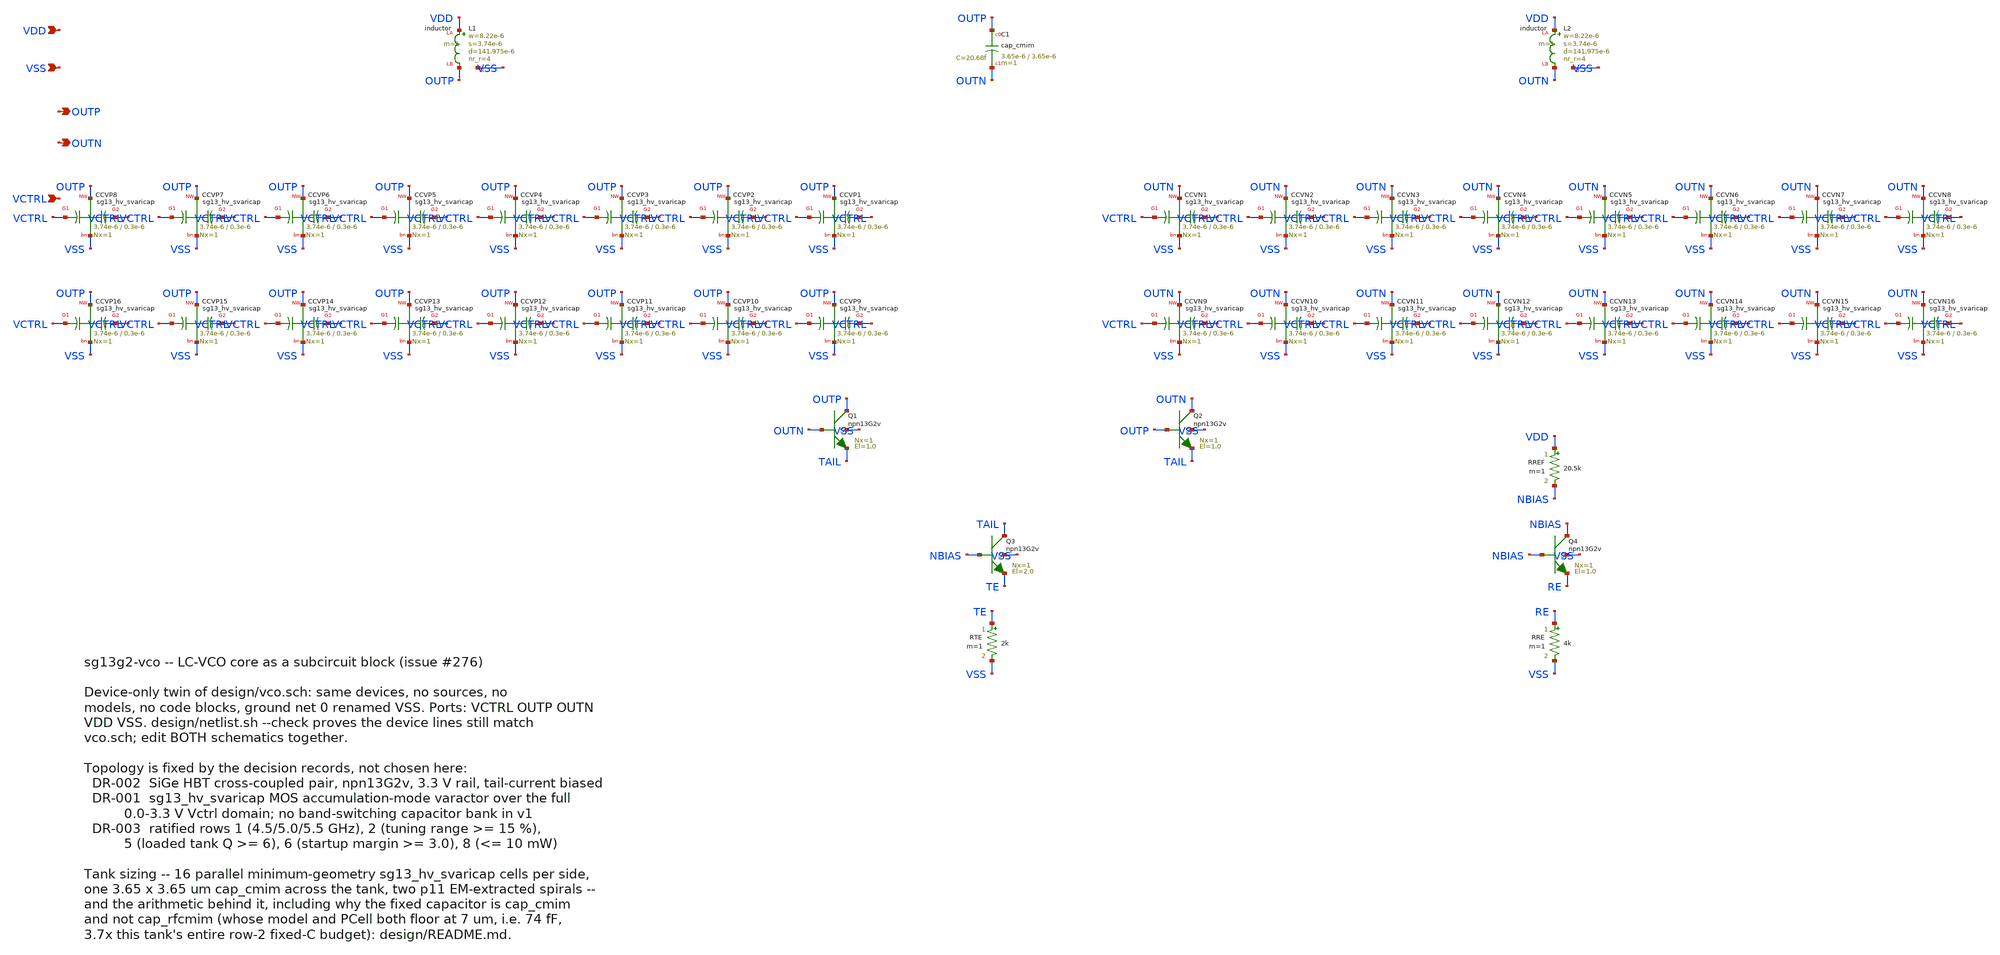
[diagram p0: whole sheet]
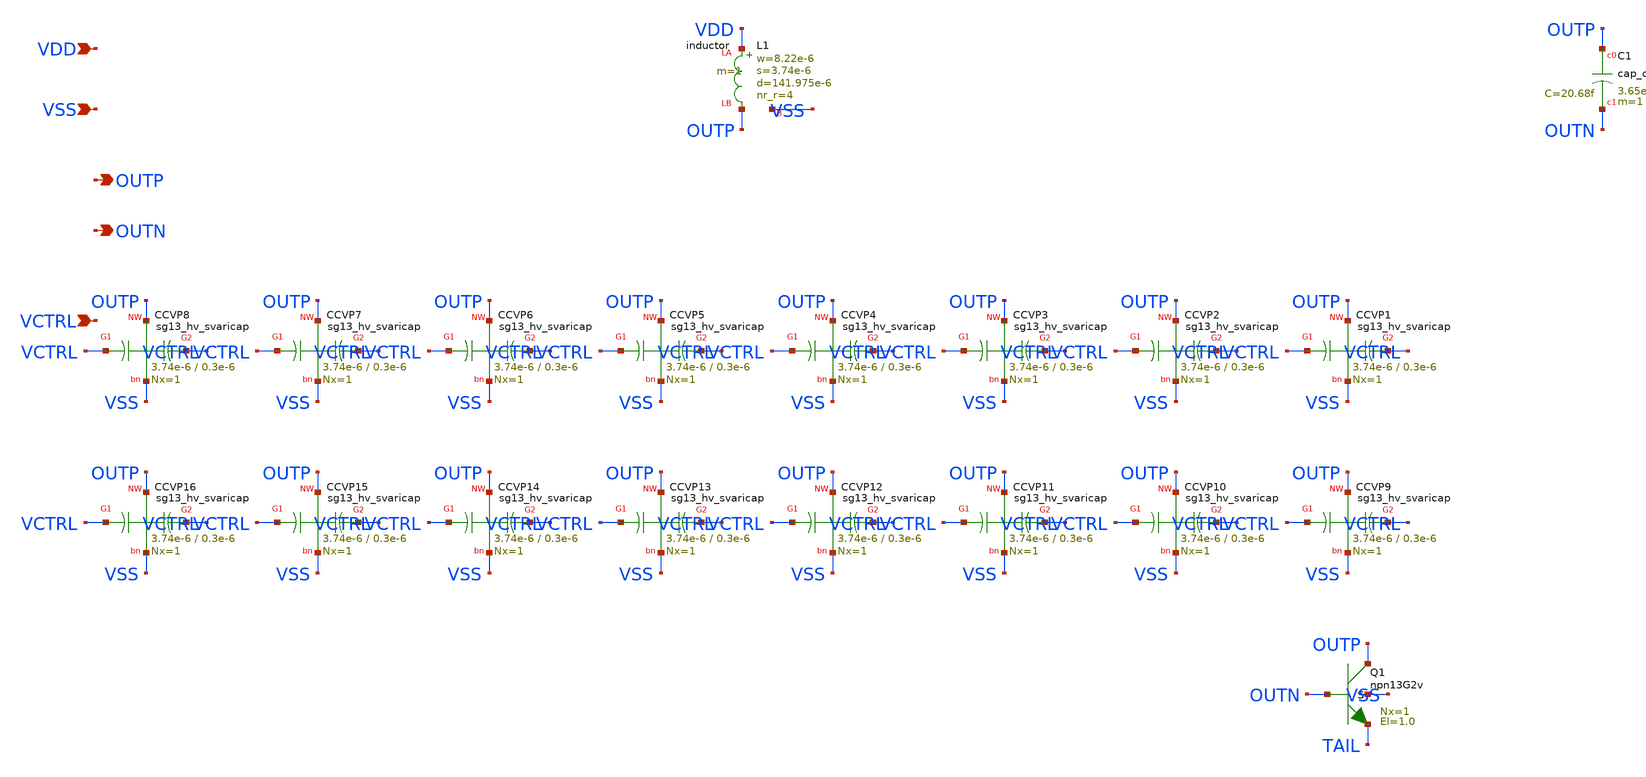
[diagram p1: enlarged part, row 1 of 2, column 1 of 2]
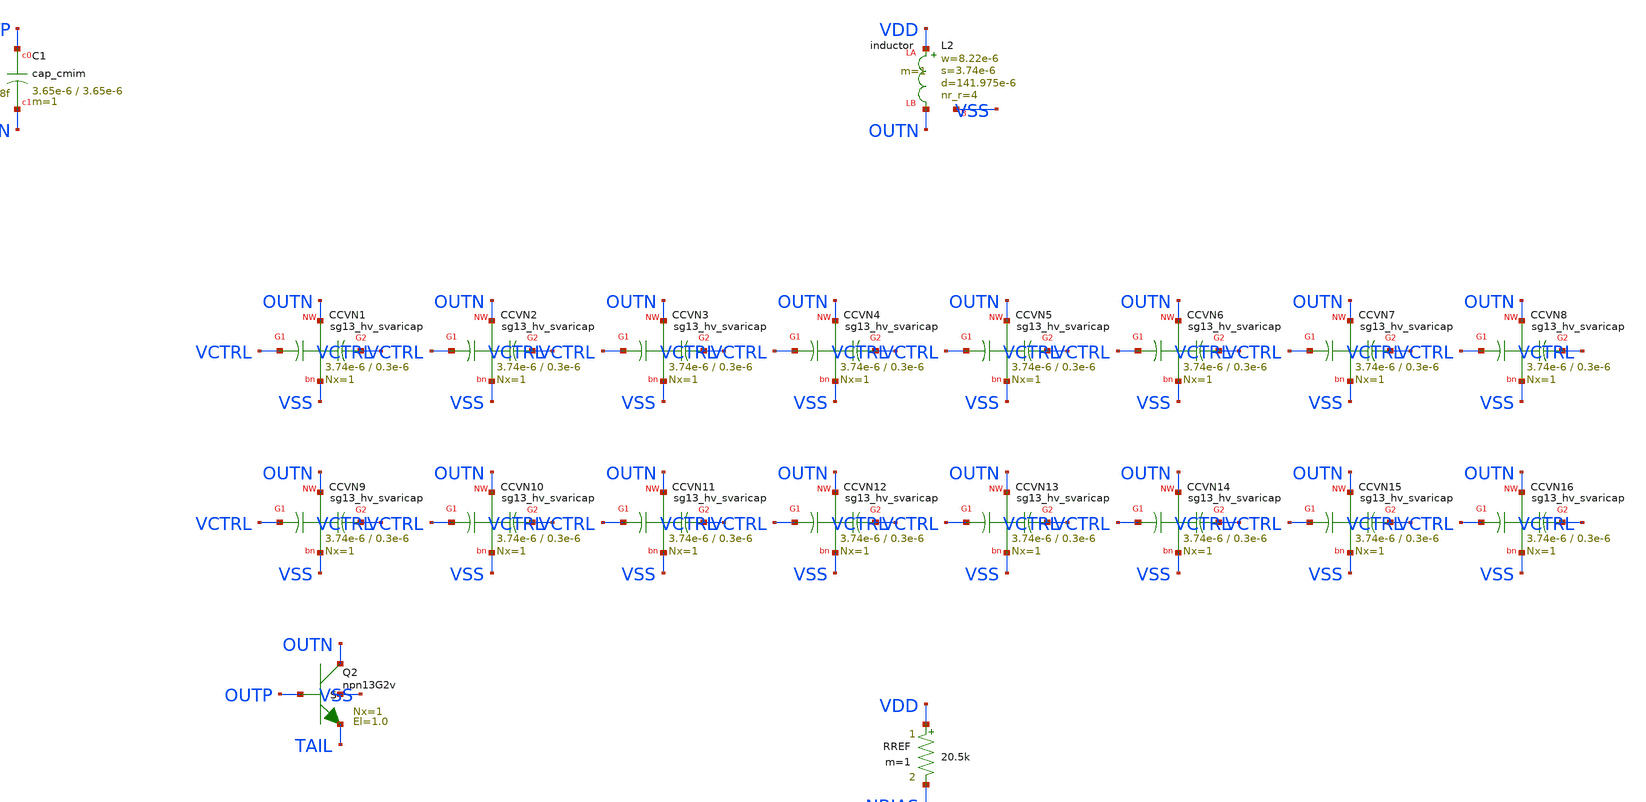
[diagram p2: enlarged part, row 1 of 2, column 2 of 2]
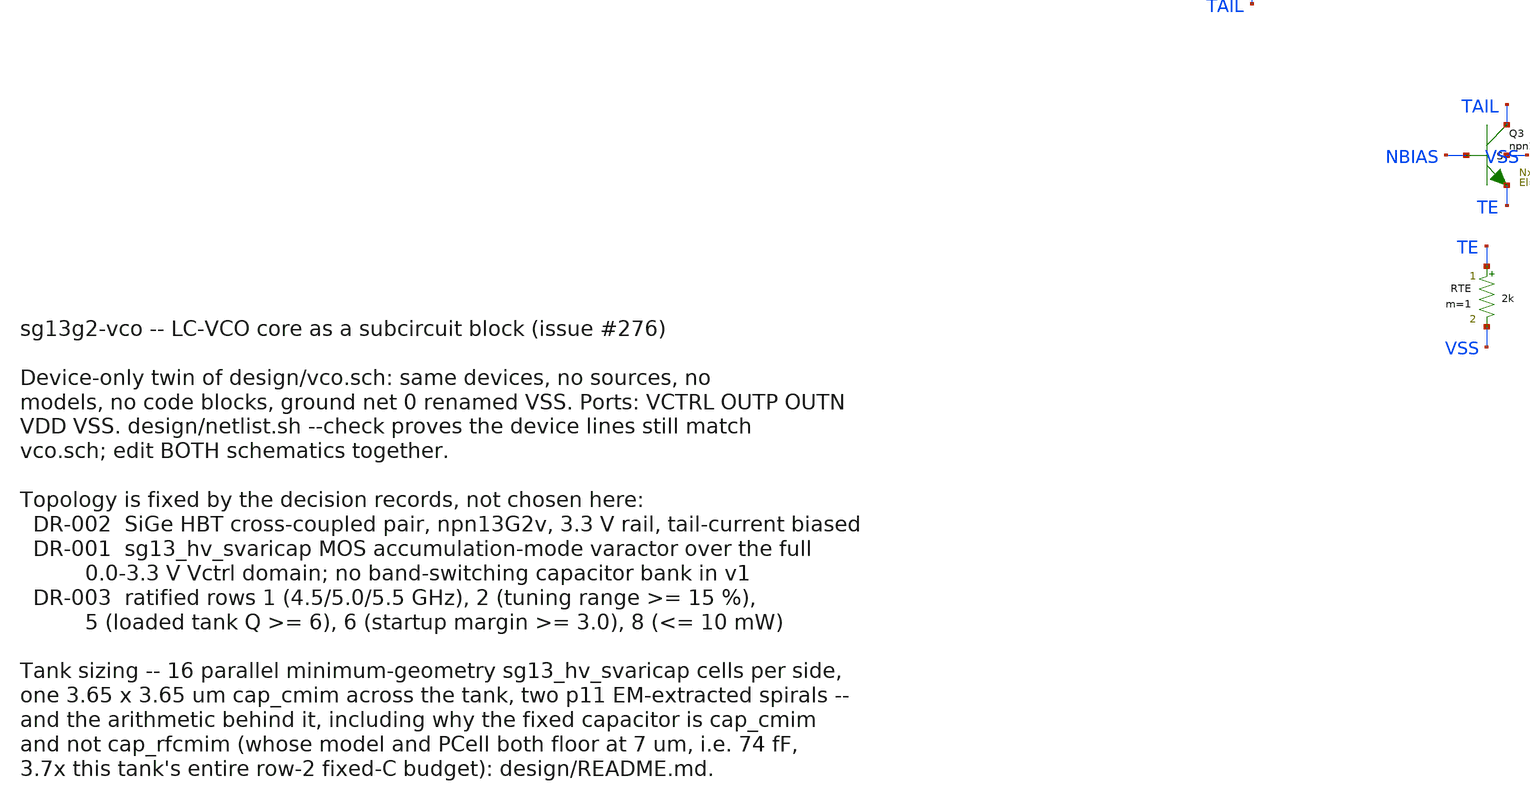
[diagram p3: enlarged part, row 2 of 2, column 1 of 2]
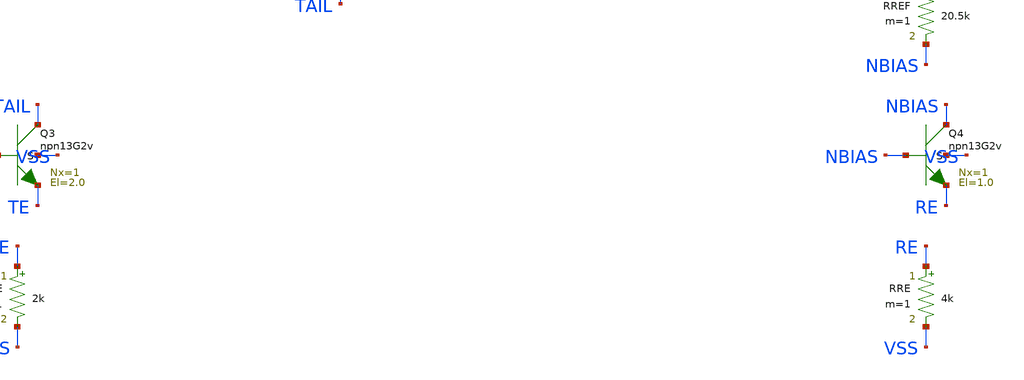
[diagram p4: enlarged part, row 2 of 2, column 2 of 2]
** sch_path: design/vco_core.sch
**.subckt vco_core VCTRL OUTP OUTN VDD VSS
*.ipin VCTRL
*.opin OUTP
*.opin OUTN
*.ipin VDD
*.ipin VSS
XL1 VDD OUTP VSS inductor w=8.22e-6 s=3.74e-6 d=141.975e-6 nr_r=4 m=1
XL2 VDD OUTN VSS inductor w=8.22e-6 s=3.74e-6 d=141.975e-6 nr_r=4 m=1
XC1 OUTP OUTN cap_cmim w=3.65e-6 l=3.65e-6 m=1 mm_ok=1
XCVP1 VCTRL OUTP VCTRL VSS sg13_hv_svaricap w=3.74e-6 l=0.3e-6 Nx=1
XCVP2 VCTRL OUTP VCTRL VSS sg13_hv_svaricap w=3.74e-6 l=0.3e-6 Nx=1
XCVP3 VCTRL OUTP VCTRL VSS sg13_hv_svaricap w=3.74e-6 l=0.3e-6 Nx=1
XCVP4 VCTRL OUTP VCTRL VSS sg13_hv_svaricap w=3.74e-6 l=0.3e-6 Nx=1
XCVP5 VCTRL OUTP VCTRL VSS sg13_hv_svaricap w=3.74e-6 l=0.3e-6 Nx=1
XCVP6 VCTRL OUTP VCTRL VSS sg13_hv_svaricap w=3.74e-6 l=0.3e-6 Nx=1
XCVP7 VCTRL OUTP VCTRL VSS sg13_hv_svaricap w=3.74e-6 l=0.3e-6 Nx=1
XCVP8 VCTRL OUTP VCTRL VSS sg13_hv_svaricap w=3.74e-6 l=0.3e-6 Nx=1
XCVP9 VCTRL OUTP VCTRL VSS sg13_hv_svaricap w=3.74e-6 l=0.3e-6 Nx=1
XCVP10 VCTRL OUTP VCTRL VSS sg13_hv_svaricap w=3.74e-6 l=0.3e-6 Nx=1
XCVP11 VCTRL OUTP VCTRL VSS sg13_hv_svaricap w=3.74e-6 l=0.3e-6 Nx=1
XCVP12 VCTRL OUTP VCTRL VSS sg13_hv_svaricap w=3.74e-6 l=0.3e-6 Nx=1
XCVP13 VCTRL OUTP VCTRL VSS sg13_hv_svaricap w=3.74e-6 l=0.3e-6 Nx=1
XCVP14 VCTRL OUTP VCTRL VSS sg13_hv_svaricap w=3.74e-6 l=0.3e-6 Nx=1
XCVP15 VCTRL OUTP VCTRL VSS sg13_hv_svaricap w=3.74e-6 l=0.3e-6 Nx=1
XCVP16 VCTRL OUTP VCTRL VSS sg13_hv_svaricap w=3.74e-6 l=0.3e-6 Nx=1
XCVN1 VCTRL OUTN VCTRL VSS sg13_hv_svaricap w=3.74e-6 l=0.3e-6 Nx=1
XCVN2 VCTRL OUTN VCTRL VSS sg13_hv_svaricap w=3.74e-6 l=0.3e-6 Nx=1
XCVN3 VCTRL OUTN VCTRL VSS sg13_hv_svaricap w=3.74e-6 l=0.3e-6 Nx=1
XCVN4 VCTRL OUTN VCTRL VSS sg13_hv_svaricap w=3.74e-6 l=0.3e-6 Nx=1
XCVN5 VCTRL OUTN VCTRL VSS sg13_hv_svaricap w=3.74e-6 l=0.3e-6 Nx=1
XCVN6 VCTRL OUTN VCTRL VSS sg13_hv_svaricap w=3.74e-6 l=0.3e-6 Nx=1
XCVN7 VCTRL OUTN VCTRL VSS sg13_hv_svaricap w=3.74e-6 l=0.3e-6 Nx=1
XCVN8 VCTRL OUTN VCTRL VSS sg13_hv_svaricap w=3.74e-6 l=0.3e-6 Nx=1
XCVN9 VCTRL OUTN VCTRL VSS sg13_hv_svaricap w=3.74e-6 l=0.3e-6 Nx=1
XCVN10 VCTRL OUTN VCTRL VSS sg13_hv_svaricap w=3.74e-6 l=0.3e-6 Nx=1
XCVN11 VCTRL OUTN VCTRL VSS sg13_hv_svaricap w=3.74e-6 l=0.3e-6 Nx=1
XCVN12 VCTRL OUTN VCTRL VSS sg13_hv_svaricap w=3.74e-6 l=0.3e-6 Nx=1
XCVN13 VCTRL OUTN VCTRL VSS sg13_hv_svaricap w=3.74e-6 l=0.3e-6 Nx=1
XCVN14 VCTRL OUTN VCTRL VSS sg13_hv_svaricap w=3.74e-6 l=0.3e-6 Nx=1
XCVN15 VCTRL OUTN VCTRL VSS sg13_hv_svaricap w=3.74e-6 l=0.3e-6 Nx=1
XCVN16 VCTRL OUTN VCTRL VSS sg13_hv_svaricap w=3.74e-6 l=0.3e-6 Nx=1
XQ1 OUTP OUTN TAIL VSS npn13G2v Nx=1 El=1.0 mm_ok=1
XQ2 OUTN OUTP TAIL VSS npn13G2v Nx=1 El=1.0 mm_ok=1
XQ3 TAIL NBIAS TE VSS npn13G2v Nx=1 El=2.0 mm_ok=1
RTE TE VSS 2k m=1
RREF VDD NBIAS 20.5k m=1
XQ4 NBIAS NBIAS RE VSS npn13G2v Nx=1 El=1.0 mm_ok=1
RRE RE VSS 4k m=1
**.ends
.end
